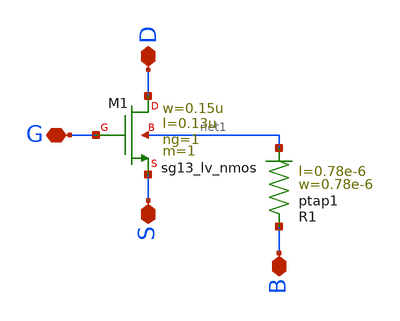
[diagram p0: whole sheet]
** sch_path: ihp-sg13cmos5l/schematic/xschem/sg13_lv_nmos_tap.sch
**.subckt sg13_lv_nmos_tap D S G B
*.iopin D
*.iopin S
*.iopin G
*.iopin B
XM1 D G S net1 sg13_lv_nmos w=0.15u l=0.13u ng=1 m=1 mm_ok=1
XR1 B net1 ptap1 R=262.8 w=0.78e-6 l=0.78e-6
**.ends
.end
